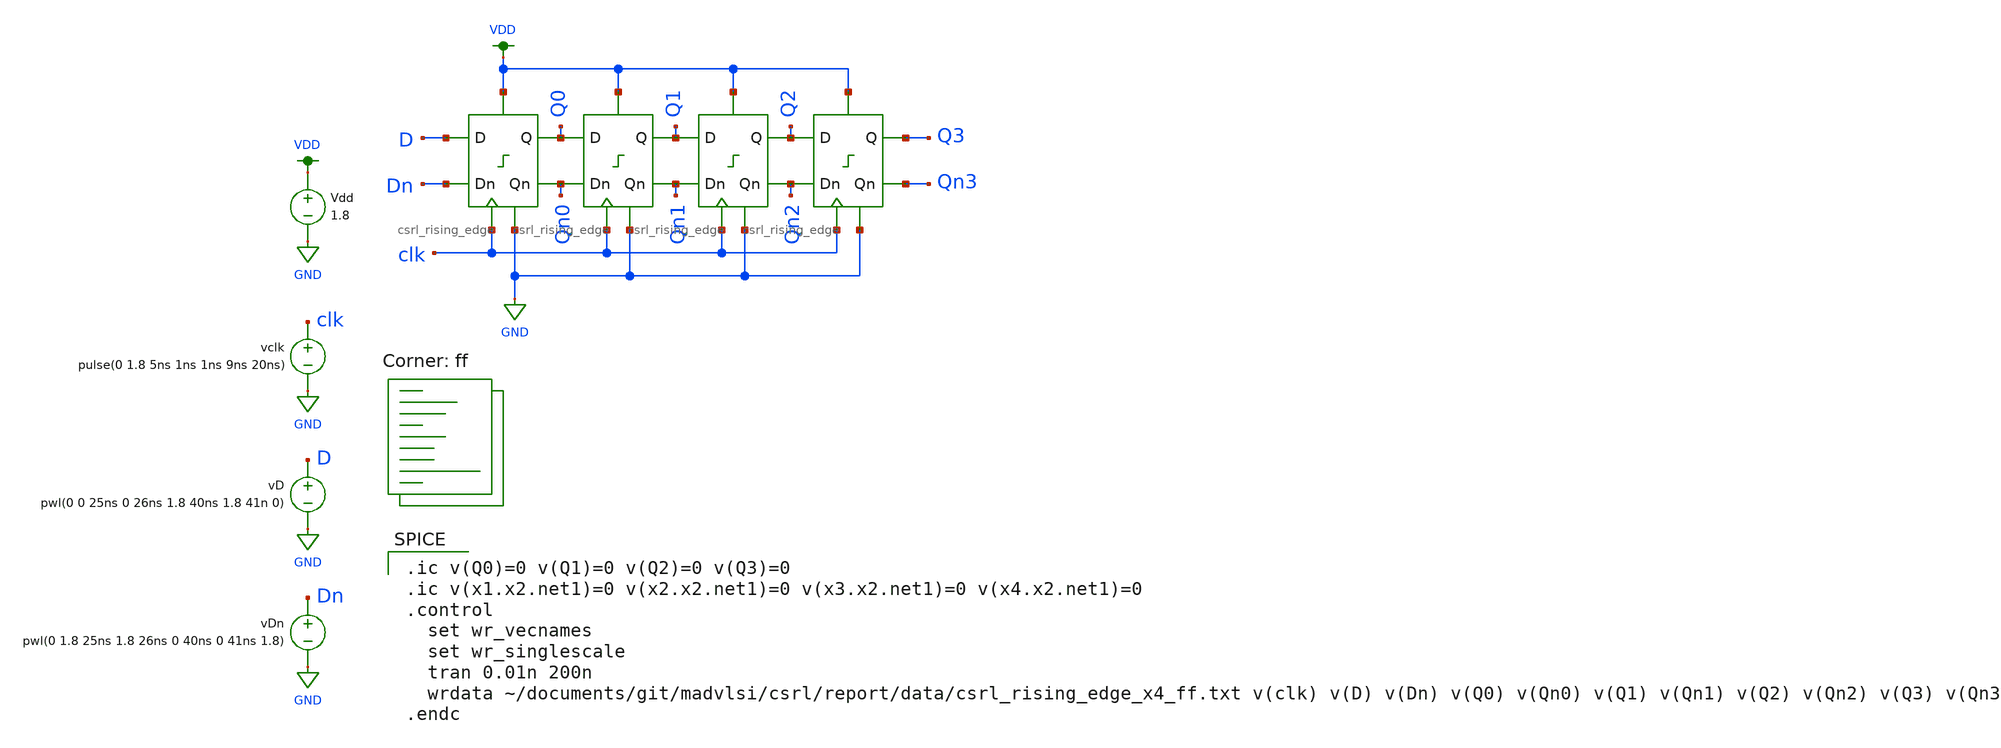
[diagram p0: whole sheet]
** sch_path: csrl/schematic/csrl_rising_edge_x4_tran.sch
**.subckt csrl_rising_edge_x4_tran
Vdd VDD GND 1.8
vclk clk GND pulse(0 1.8 5ns 1ns 1ns 9ns 20ns)
vD D GND pwl(0 0 25ns 0 26ns 1.8 40ns 1.8 41n 0)
vDn Dn GND pwl(0 1.8 25ns 1.8 26ns 0 40ns 0 41ns 1.8)
X1 D Dn Qn0 Q0 GND clk VDD csrl_rising_edge
X2 Q0 Qn0 Qn1 Q1 GND clk VDD csrl_rising_edge
X3 Q1 Qn1 Qn2 Q2 GND clk VDD csrl_rising_edge
X4 Q2 Qn2 Qn3 Q3 GND clk VDD csrl_rising_edge
**** begin user architecture code

.ic v(Q0)=0 v(Q1)=0 v(Q2)=0 v(Q3)=0
.ic v(x1.x2.net1)=0 v(x2.x2.net1)=0 v(x3.x2.net1)=0 v(x4.x2.net1)=0
.control
  set wr_vecnames
  set wr_singlescale
  tran 0.01n 200n
  wrdata ~/documents/git/madvlsi/csrl/report/data/csrl_rising_edge_x4_ff.txt v(clk) v(D) v(Dn) v(Q0)
+ v(Qn0) v(Q1) v(Qn1) v(Q2) v(Qn2) v(Q3) v(Qn3)
.endc

.lib $::SKYWATER_MODELS/sky130.lib.spice ff
**** end user architecture code
**.ends
.GLOBAL GND
.GLOBAL VDD
.end
